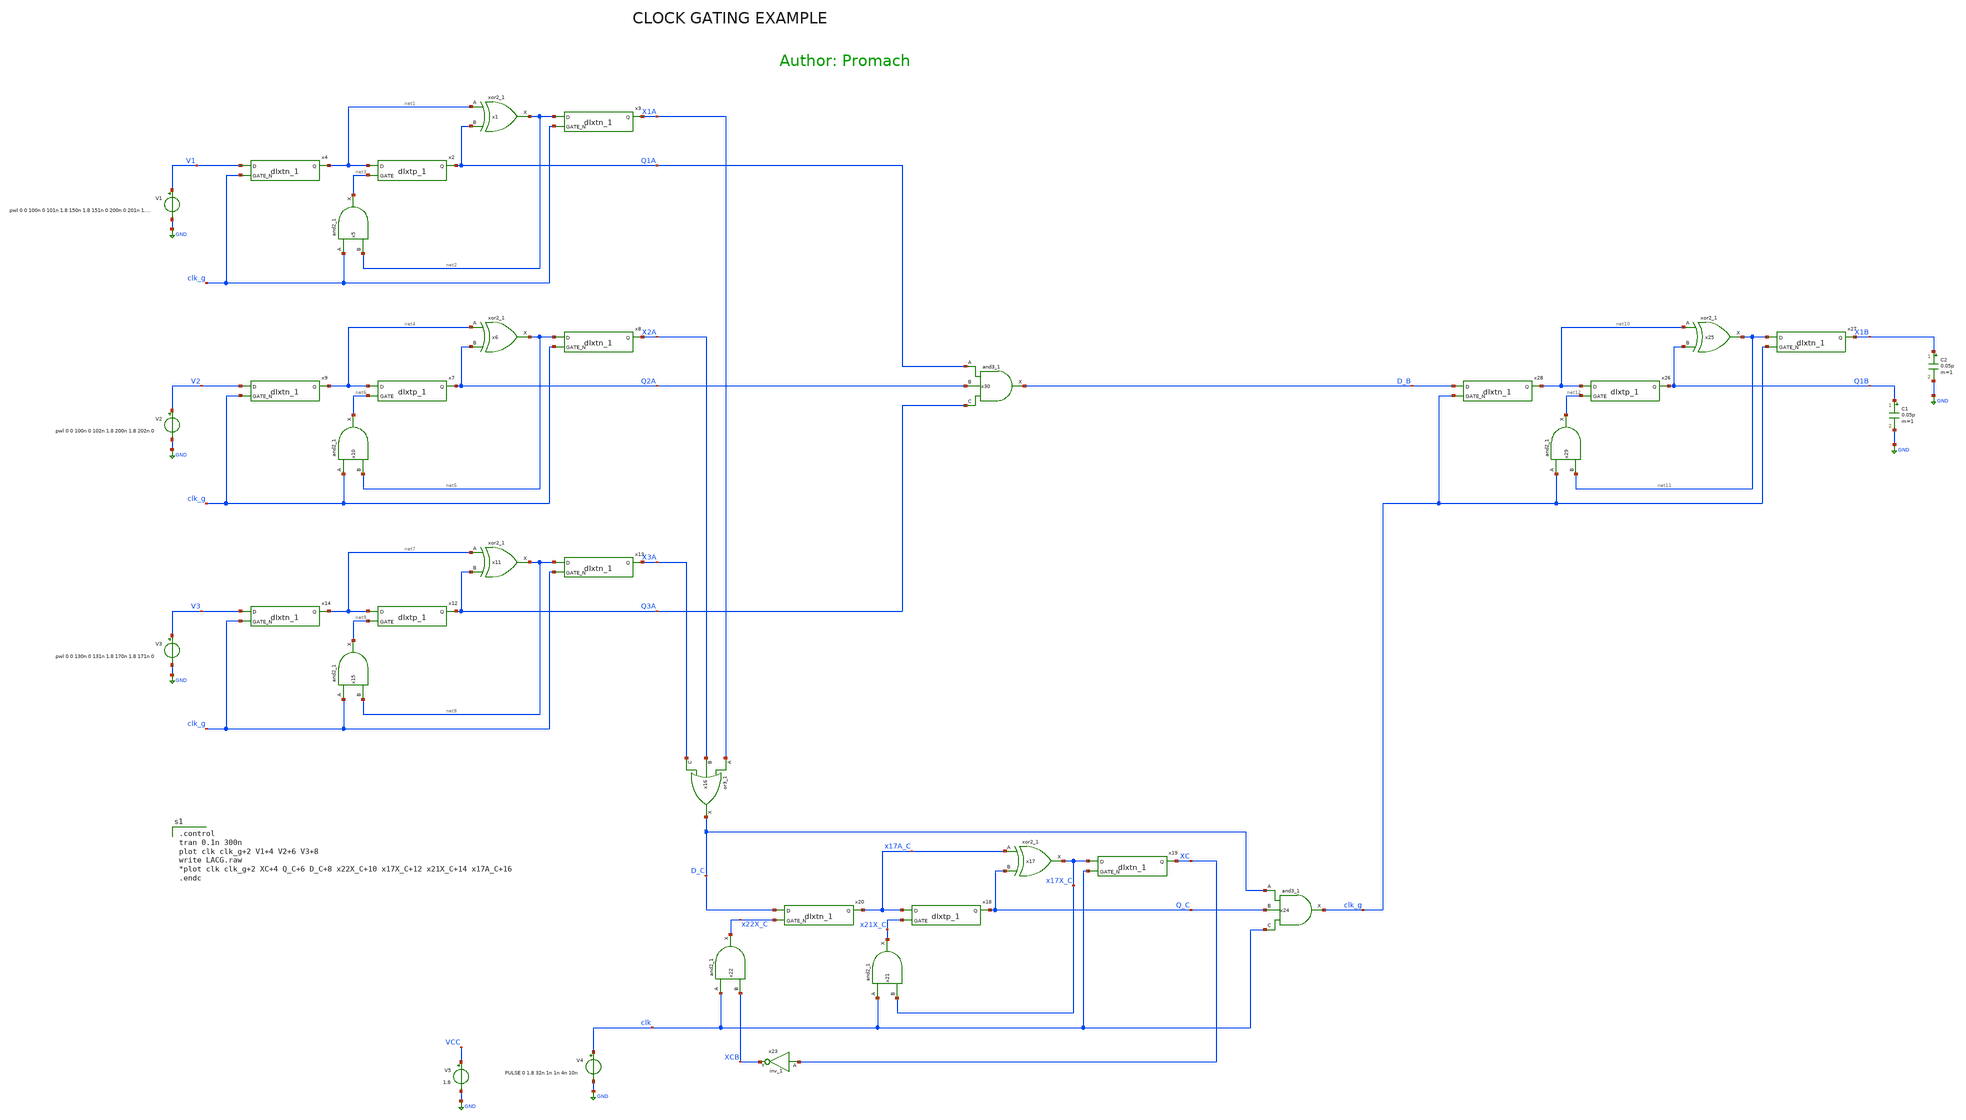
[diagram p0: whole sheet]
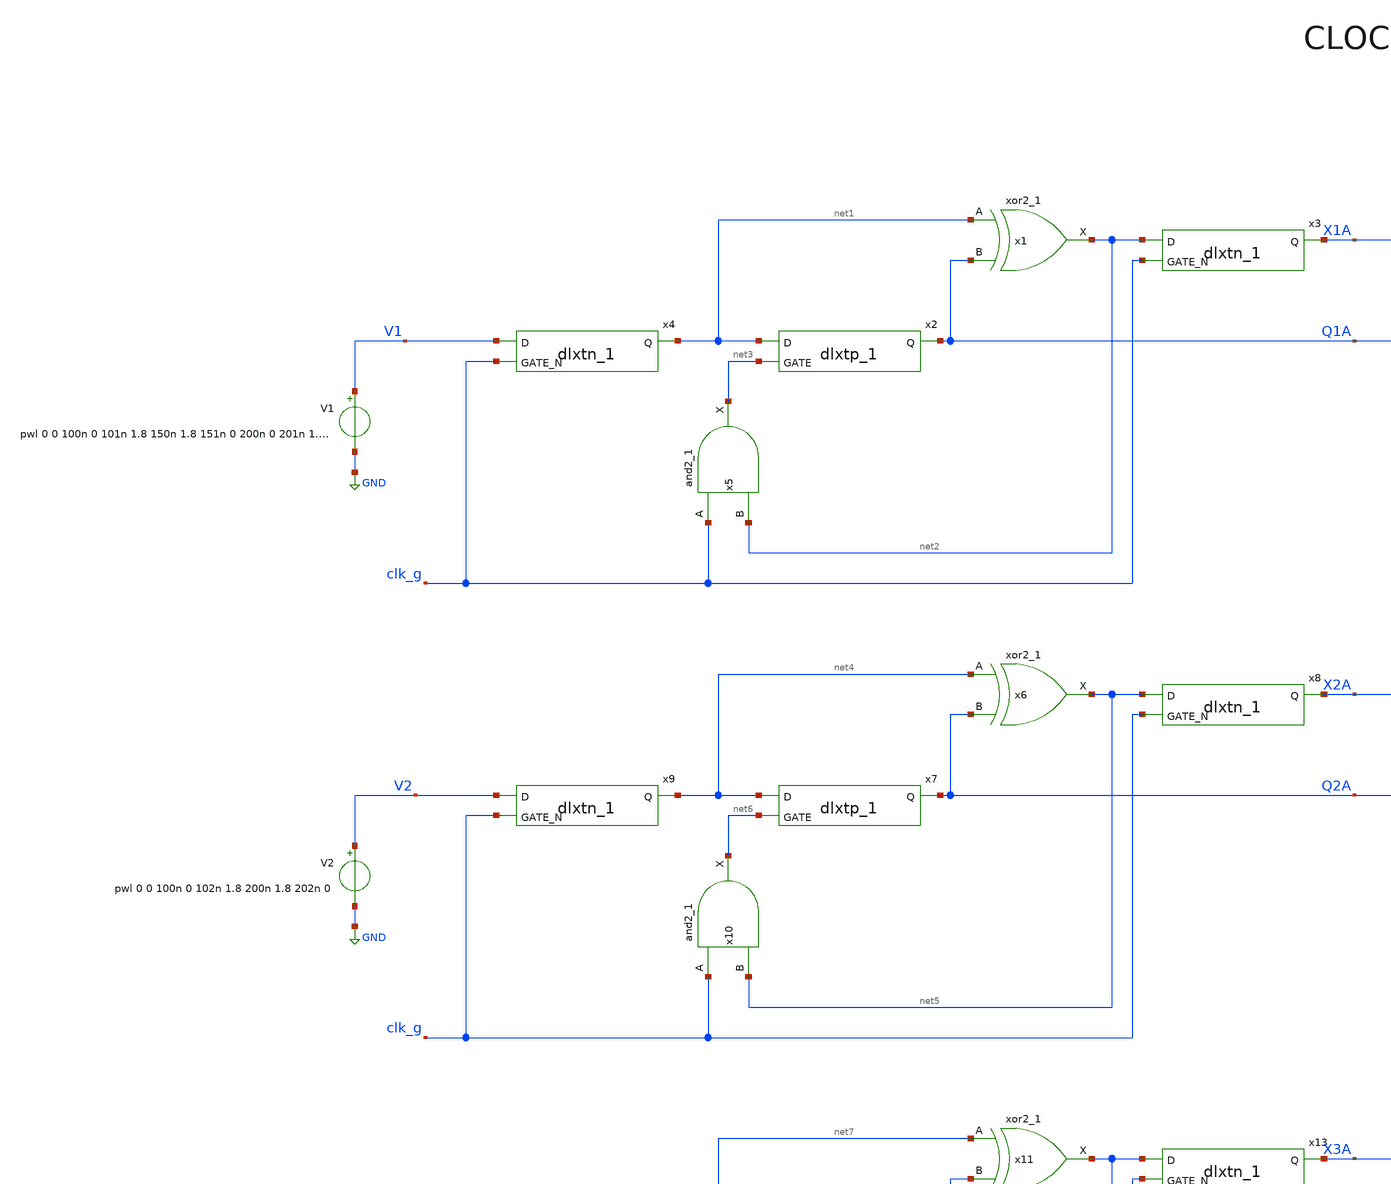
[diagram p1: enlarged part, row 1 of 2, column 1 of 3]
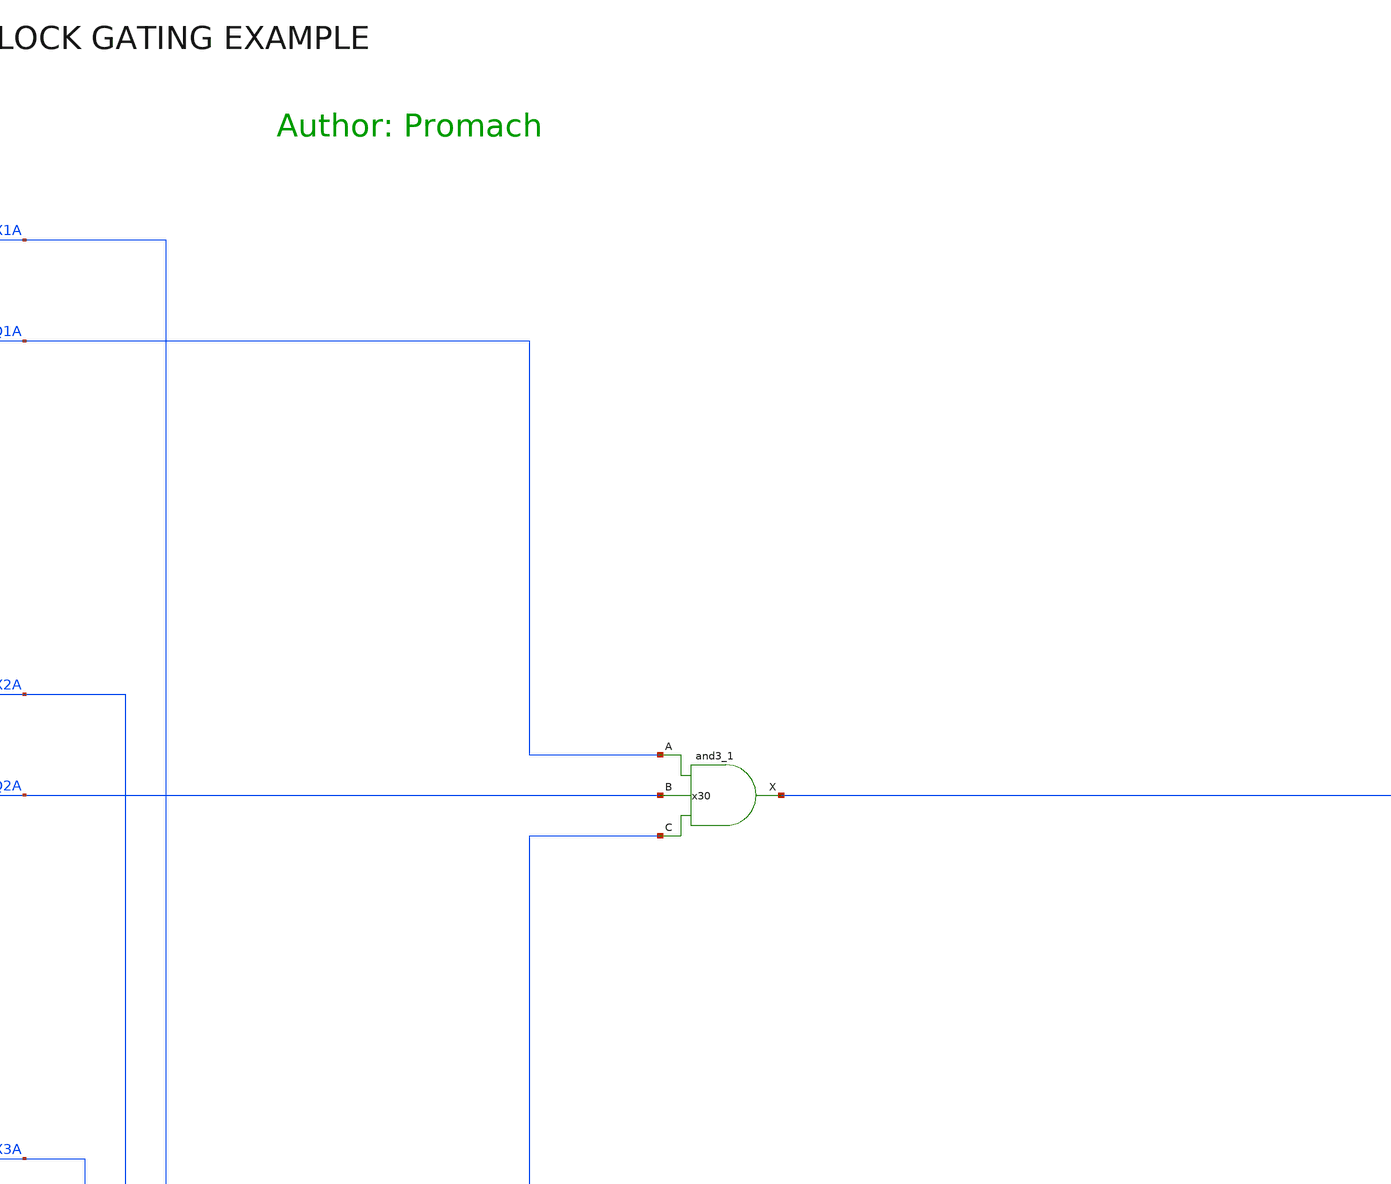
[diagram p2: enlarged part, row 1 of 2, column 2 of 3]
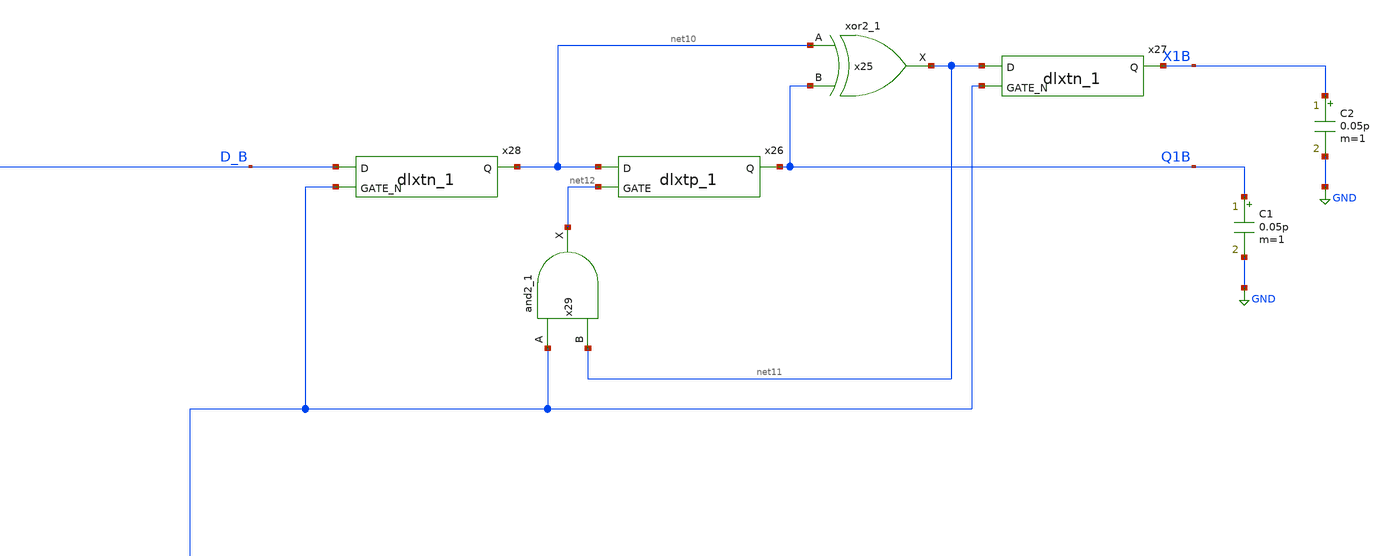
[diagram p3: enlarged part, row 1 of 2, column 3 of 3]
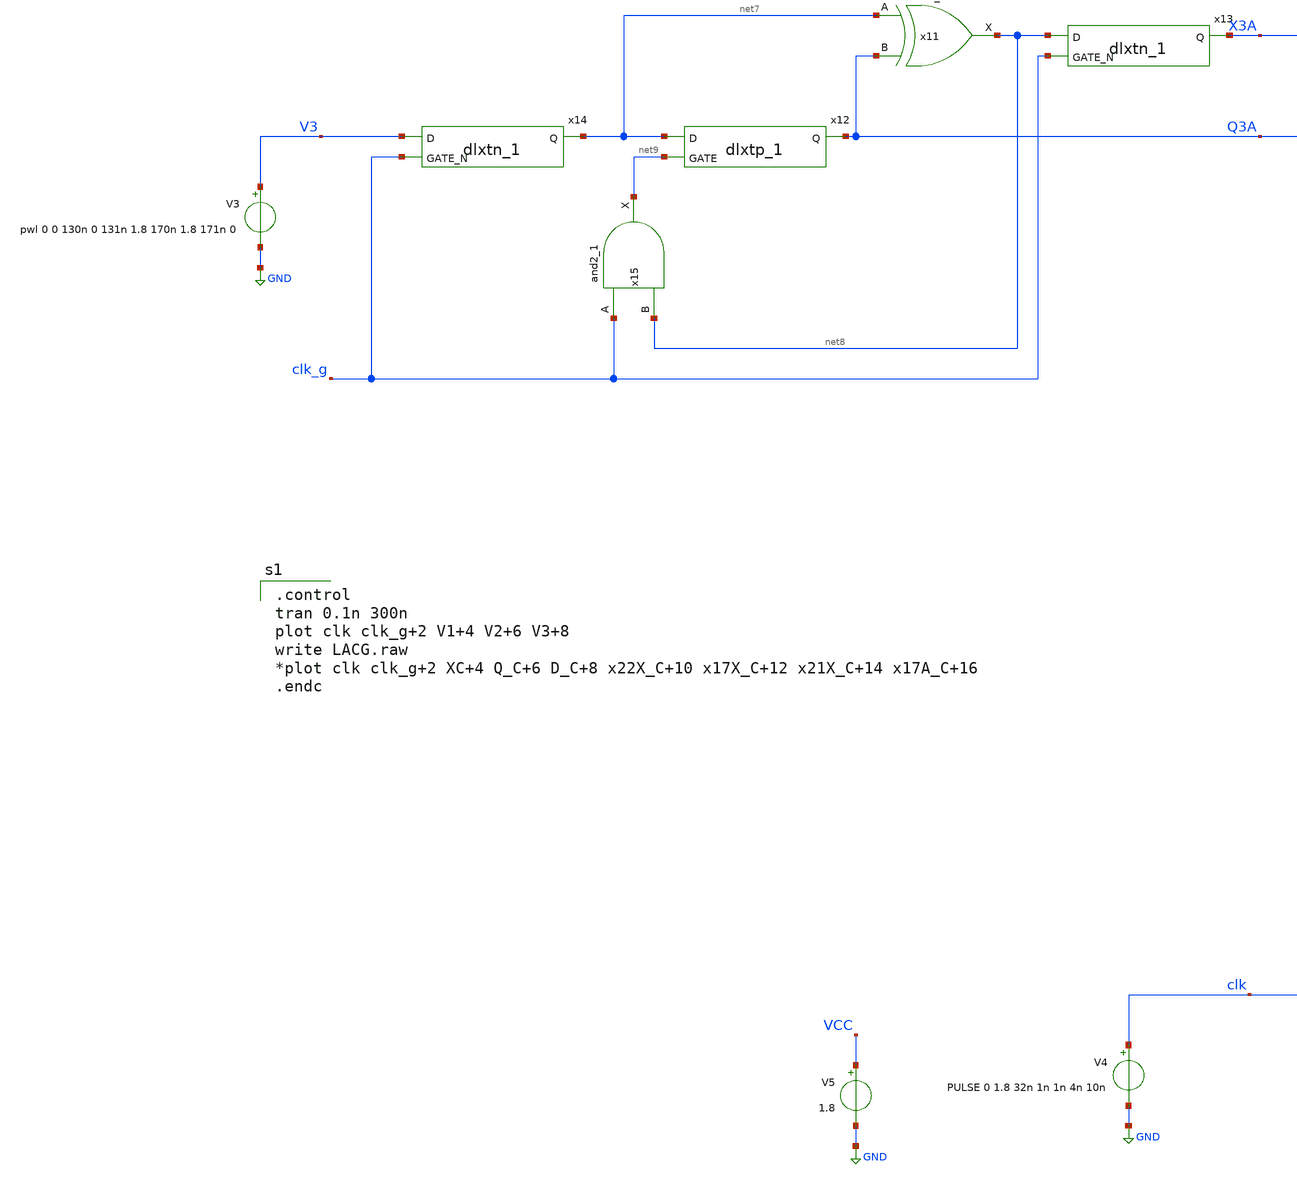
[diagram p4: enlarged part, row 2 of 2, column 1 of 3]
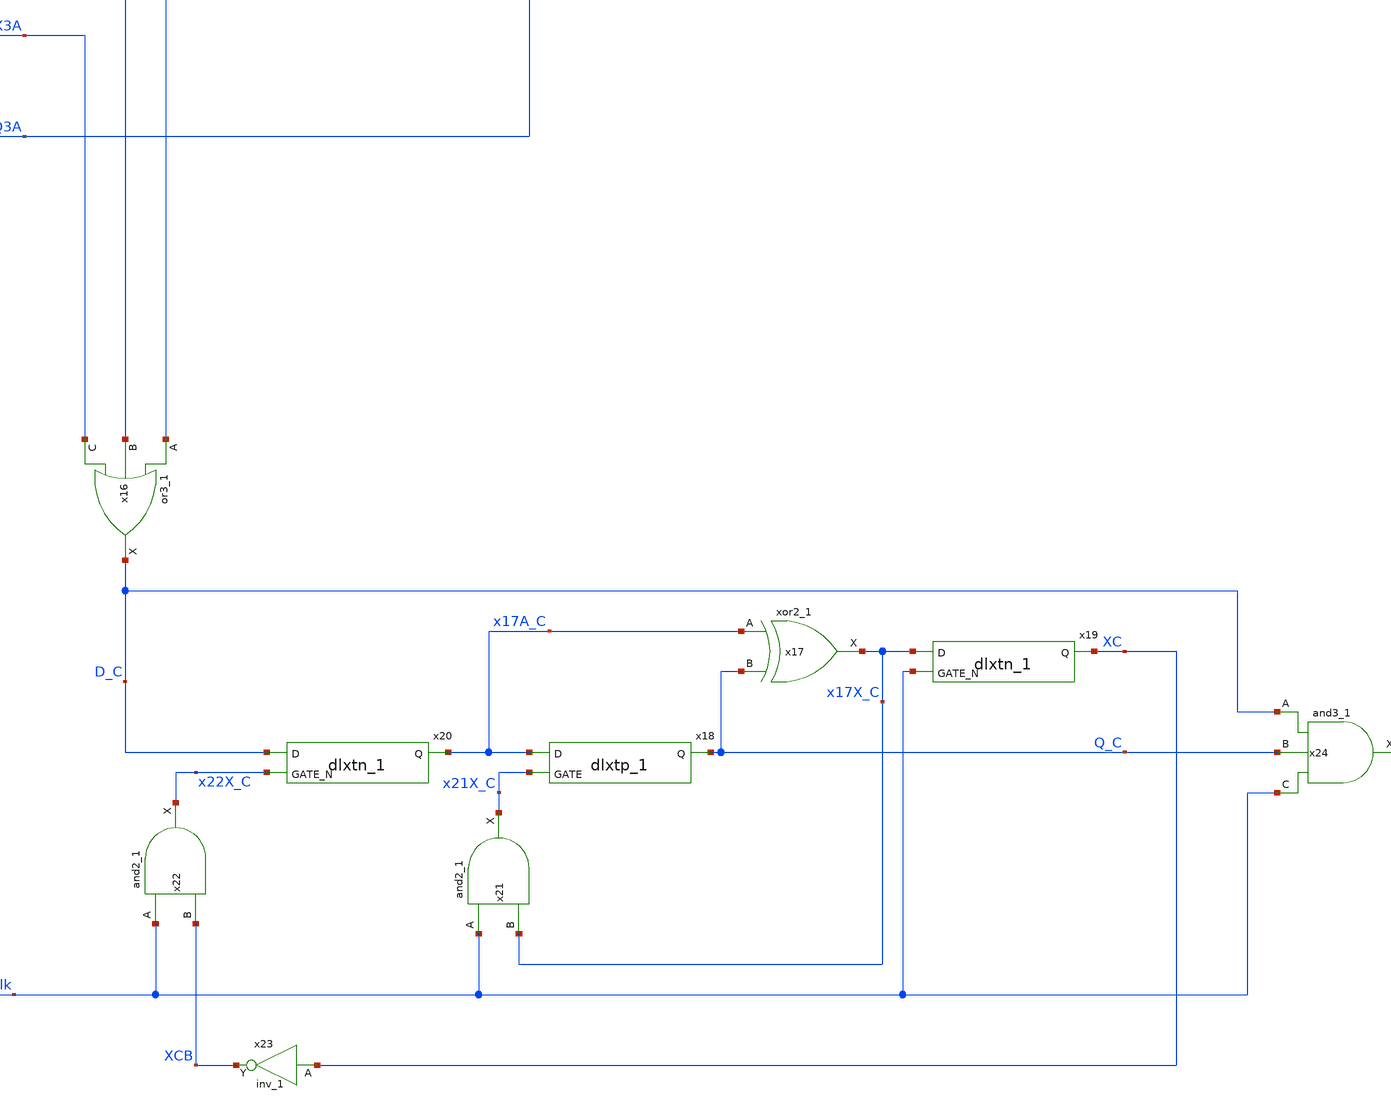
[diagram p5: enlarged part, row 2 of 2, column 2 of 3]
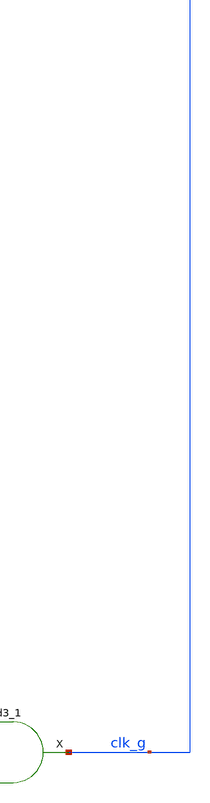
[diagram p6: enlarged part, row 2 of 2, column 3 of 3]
** sch_path: xyce/sky130A-xyce/libs.tech/xschem/sky130_tests/LACG.sch
**.subckt LACG
x1 net1 Q1A GND GND VCC VCC net2 sky130_fd_sc_hd__xor2_1
x2 net1 net3 GND GND VCC VCC Q1A sky130_fd_sc_hd__dlxtp_1
x3 net2 clk_g GND GND VCC VCC X1A sky130_fd_sc_hd__dlxtn_1
x4 V1 clk_g GND GND VCC VCC net1 sky130_fd_sc_hd__dlxtn_1
x5 clk_g net2 GND GND VCC VCC net3 sky130_fd_sc_hd__and2_1
V1 V1 GND pwl 0 0 100n 0 101n 1.8 150n 1.8 151n 0 200n 0 201n 1.8 231n 1.8
x6 net4 Q2A GND GND VCC VCC net5 sky130_fd_sc_hd__xor2_1
x7 net4 net6 GND GND VCC VCC Q2A sky130_fd_sc_hd__dlxtp_1
x8 net5 clk_g GND GND VCC VCC X2A sky130_fd_sc_hd__dlxtn_1
x9 V2 clk_g GND GND VCC VCC net4 sky130_fd_sc_hd__dlxtn_1
x10 clk_g net5 GND GND VCC VCC net6 sky130_fd_sc_hd__and2_1
x11 net7 Q3A GND GND VCC VCC net8 sky130_fd_sc_hd__xor2_1
x12 net7 net9 GND GND VCC VCC Q3A sky130_fd_sc_hd__dlxtp_1
x13 net8 clk_g GND GND VCC VCC X3A sky130_fd_sc_hd__dlxtn_1
x14 V3 clk_g GND GND VCC VCC net7 sky130_fd_sc_hd__dlxtn_1
x15 clk_g net8 GND GND VCC VCC net9 sky130_fd_sc_hd__and2_1
V2 V2 GND pwl 0 0 100n 0 102n 1.8 200n 1.8 202n 0
V3 V3 GND pwl 0 0 130n 0 131n 1.8 170n 1.8 171n 0
x17 x17A_C Q_C GND GND VCC VCC x17X_C sky130_fd_sc_hd__xor2_1
x18 x17A_C x21X_C GND GND VCC VCC Q_C sky130_fd_sc_hd__dlxtp_1
x19 x17X_C clk GND GND VCC VCC XC sky130_fd_sc_hd__dlxtn_1
x20 D_C x22X_C GND GND VCC VCC x17A_C sky130_fd_sc_hd__dlxtn_1
x21 clk x17X_C GND GND VCC VCC x21X_C sky130_fd_sc_hd__and2_1
x22 clk XCB GND GND VCC VCC x22X_C sky130_fd_sc_hd__and2_1
x23 XC GND GND VCC VCC XCB sky130_fd_sc_hd__inv_1
x24 D_C Q_C clk GND GND VCC VCC clk_g sky130_fd_sc_hd__and3_1
x25 net10 Q1B GND GND VCC VCC net11 sky130_fd_sc_hd__xor2_1
x26 net10 net12 GND GND VCC VCC Q1B sky130_fd_sc_hd__dlxtp_1
x27 net11 clk_g GND GND VCC VCC X1B sky130_fd_sc_hd__dlxtn_1
x28 D_B clk_g GND GND VCC VCC net10 sky130_fd_sc_hd__dlxtn_1
x29 clk_g net11 GND GND VCC VCC net12 sky130_fd_sc_hd__and2_1
C1 Q1B GND 0.05p m=1
C2 X1B GND 0.05p m=1
V4 clk GND PULSE 0 1.8 32n 1n 1n 4n 10n
V5 VCC GND 1.8
x16 X1A X2A X3A GND GND VCC VCC D_C sky130_fd_sc_hd__or3_1
x30 Q1A Q2A Q3A GND GND VCC VCC D_B sky130_fd_sc_hd__and3_1
**** begin user architecture code

.control
tran 0.1n 300n
plot clk clk_g+2 V1+4 V2+6 V3+8
write LACG.raw
*plot clk clk_g+2 XC+4 Q_C+6 D_C+8 x22X_C+10 x17X_C+12 x21X_C+14 x17A_C+16
.endc



[sky130_models]


*.include $::SKYWATER_MODELS/models/sky130.lib.spice tt


.include $::SKYWATER_MODELS/cells/nfet_01v8/sky130_fd_pr__nfet_01v8__tt.corner.spice
.include $::SKYWATER_MODELS/cells/nfet_01v8_lvt/sky130_fd_pr__nfet_01v8_lvt__tt.corner.spice
.include $::SKYWATER_MODELS/cells/pfet_01v8/sky130_fd_pr__pfet_01v8__tt.corner.spice
.include $::SKYWATER_MODELS/cells/nfet_03v3_nvt/sky130_fd_pr__nfet_03v3_nvt__tt.corner.spice
.include $::SKYWATER_MODELS/cells/nfet_05v0_nvt/sky130_fd_pr__nfet_05v0_nvt__tt.corner.spice
.include $::SKYWATER_MODELS/cells/esd_nfet_01v8/sky130_fd_pr__esd_nfet_01v8__tt.corner.spice
.include $::SKYWATER_MODELS/cells/pfet_01v8_lvt/sky130_fd_pr__pfet_01v8_lvt__tt.corner.spice
.include $::SKYWATER_MODELS/cells/pfet_01v8_hvt/sky130_fd_pr__pfet_01v8_hvt__tt.corner.spice
.include $::SKYWATER_MODELS/cells/esd_pfet_g5v0d10v5/sky130_fd_pr__esd_pfet_g5v0d10v5__tt.corner.spice
.include $::SKYWATER_MODELS/cells/pfet_g5v0d10v5/sky130_fd_pr__pfet_g5v0d10v5__tt.corner.spice
.include $::SKYWATER_MODELS/cells/pfet_g5v0d16v0/sky130_fd_pr__pfet_g5v0d16v0__tt.corner.spice
.include $::SKYWATER_MODELS/cells/nfet_g5v0d10v5/sky130_fd_pr__nfet_g5v0d10v5__tt.corner.spice
.include $::SKYWATER_MODELS/cells/nfet_g5v0d16v0/sky130_fd_pr__nfet_g5v0d16v0__tt_discrete.corner.spice
.include $::SKYWATER_MODELS/cells/esd_nfet_g5v0d10v5/sky130_fd_pr__esd_nfet_g5v0d10v5__tt.corner.spice
.include $::SKYWATER_MODELS/models/corners/tt/nonfet.spice
* Mismatch parameters
.include $::SKYWATER_MODELS/cells/nfet_01v8/sky130_fd_pr__nfet_01v8__mismatch.corner.spice
.include $::SKYWATER_MODELS/cells/pfet_01v8/sky130_fd_pr__pfet_01v8__mismatch.corner.spice
.include $::SKYWATER_MODELS/cells/nfet_01v8_lvt/sky130_fd_pr__nfet_01v8_lvt__mismatch.corner.spice
.include $::SKYWATER_MODELS/cells/pfet_01v8_lvt/sky130_fd_pr__pfet_01v8_lvt__mismatch.corner.spice
.include $::SKYWATER_MODELS/cells/pfet_01v8_hvt/sky130_fd_pr__pfet_01v8_hvt__mismatch.corner.spice
.include $::SKYWATER_MODELS/cells/nfet_g5v0d10v5/sky130_fd_pr__nfet_g5v0d10v5__mismatch.corner.spice
.include $::SKYWATER_MODELS/cells/pfet_g5v0d10v5/sky130_fd_pr__pfet_g5v0d10v5__mismatch.corner.spice
.include $::SKYWATER_MODELS/cells/nfet_05v0_nvt/sky130_fd_pr__nfet_05v0_nvt__mismatch.corner.spice
.include $::SKYWATER_MODELS/cells/nfet_03v3_nvt/sky130_fd_pr__nfet_03v3_nvt__mismatch.corner.spice
* Resistor$::SKYWATER_MODELS/Capacitor
.include $::SKYWATER_MODELS/models/r+c/res_typical__cap_typical.spice
.include $::SKYWATER_MODELS/models/r+c/res_typical__cap_typical__lin.spice
* Special cells
.include $::SKYWATER_MODELS/models/corners/tt/specialized_cells.spice
* All models
.include $::SKYWATER_MODELS/models/all.spice
* Corner
.include $::SKYWATER_MODELS/models/corners/tt/rf.spice

**** end user architecture code
**.ends
.GLOBAL GND
.end
